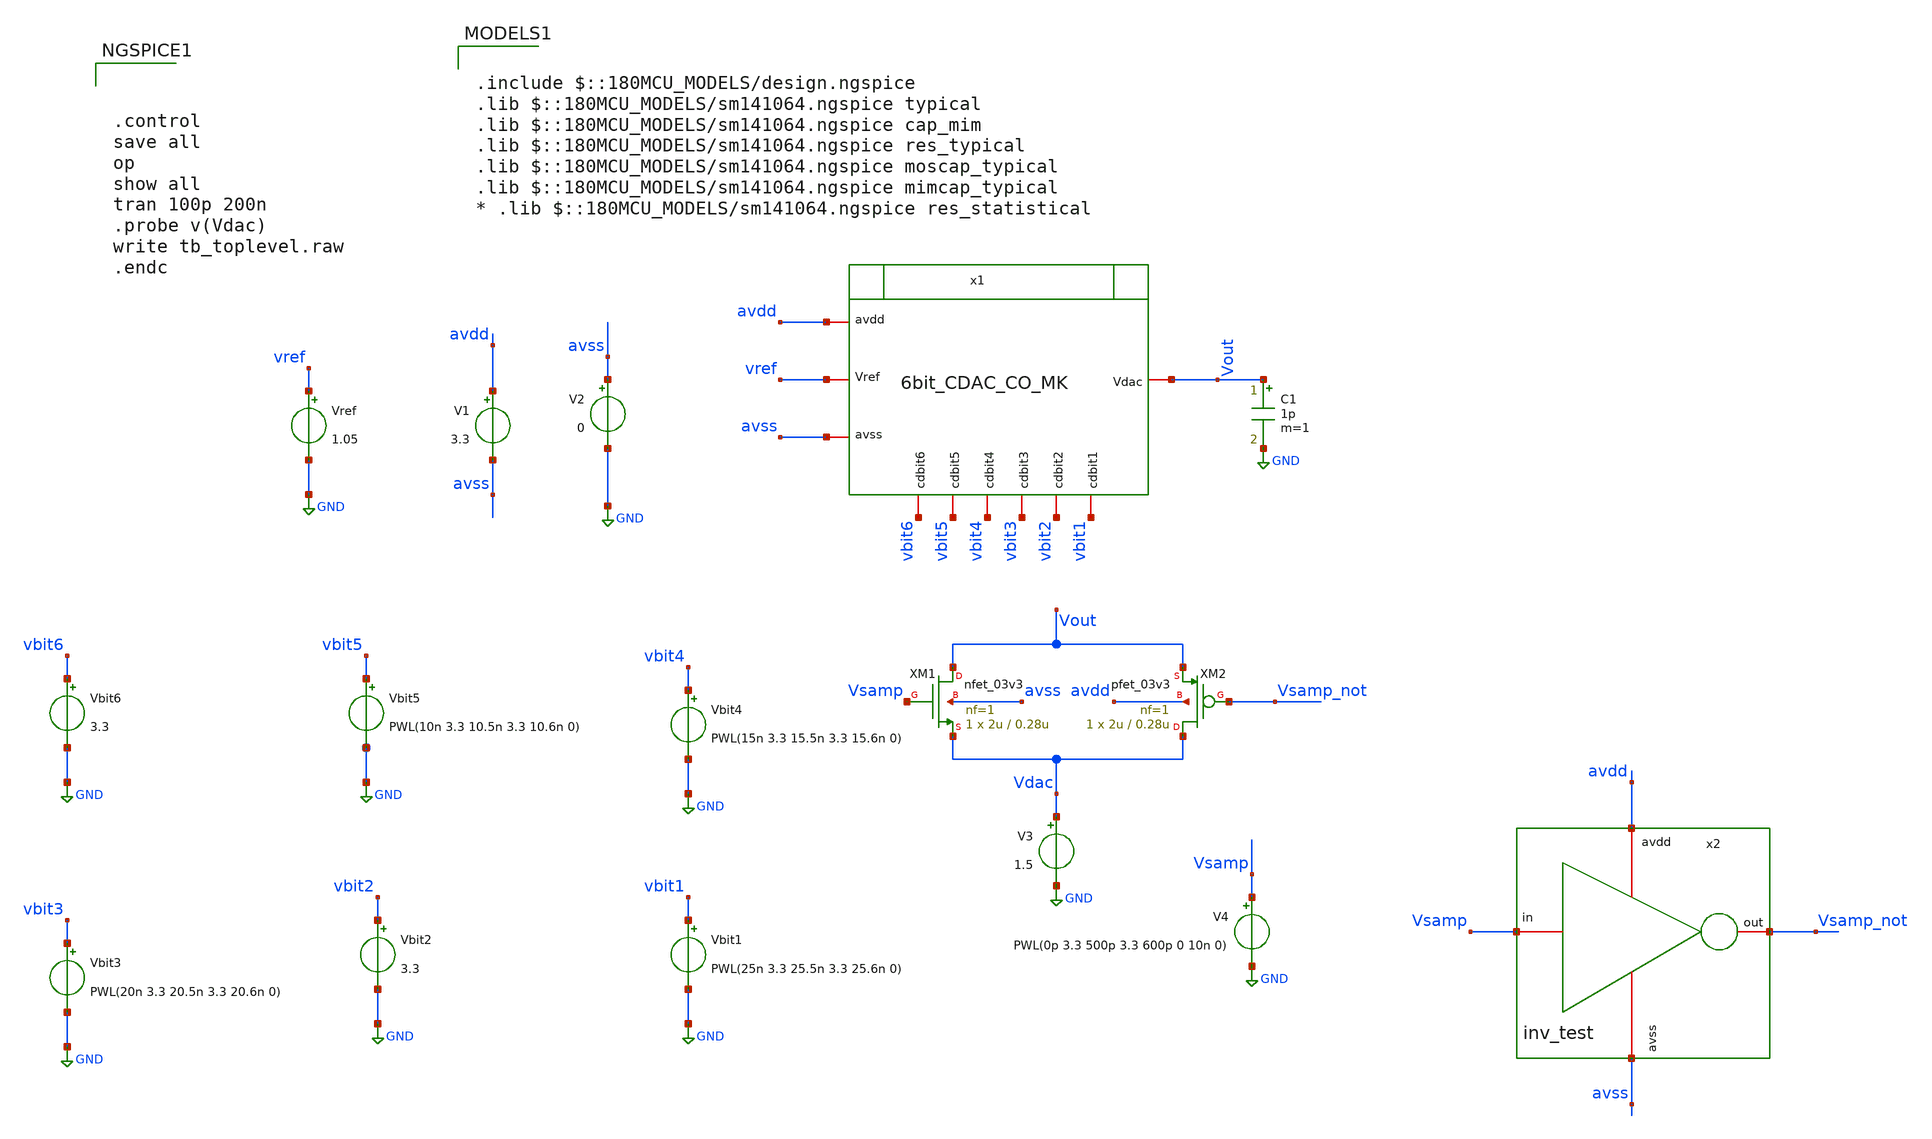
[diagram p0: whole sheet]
** sch_path: designs/full_ADC/tb_toplevel.sch
**.subckt tb_toplevel
V1 avdd avss 3.3
V2 avss GND 0
Vbit1 vbit1 GND PWL(25n 3.3 25.5n 3.3 25.6n 0)
Vbit2 vbit2 GND 3.3
Vbit3 vbit3 GND PWL(20n 3.3 20.5n 3.3 20.6n 0)
Vbit4 vbit4 GND PWL(15n 3.3 15.5n 3.3 15.6n 0)
Vbit5 vbit5 GND PWL(10n 3.3 10.5n 3.3 10.6n 0)
Vbit6 vbit6 GND 3.3
Vref vref GND 1.05
C1 Vout GND 1p m=1
V3 Vdac GND 1.5
XM1 Vout Vsamp Vdac avss nfet_03v3 L=0.28u W=2u nf=1 ad='int((nf+1)/2) * W/nf * 0.18u' as='int((nf+2)/2) * W/nf * 0.18u'
+ pd='2*int((nf+1)/2) * (W/nf + 0.18u)' ps='2*int((nf+2)/2) * (W/nf + 0.18u)' nrd='0.18u / W' nrs='0.18u / W'
+ sa=0 sb=0 sd=0 m=1
XM2 Vdac Vsamp_not Vout avdd pfet_03v3 L=0.28u W=2u nf=1 ad='int((nf+1)/2) * W/nf * 0.18u' as='int((nf+2)/2) * W/nf * 0.18u'
+ pd='2*int((nf+1)/2) * (W/nf + 0.18u)' ps='2*int((nf+2)/2) * (W/nf + 0.18u)' nrd='0.18u / W' nrs='0.18u / W'
+ sa=0 sb=0 sd=0 m=1
x2 avdd Vsamp Vsamp_not avss inv_test
V4 Vsamp GND PWL(0p 3.3 500p 3.3 600p 0 10n 0)
x1 Vout avdd avss vref vbit6 vbit5 vbit3 vbit1 vbit2 vbit4 6bit_CDAC_CO_MK
**** begin user architecture code



.control
save all
op
show all
tran 100p 200n
.probe v(Vdac)
write tb_toplevel.raw
.endc



.include $::180MCU_MODELS/design.ngspice
.lib $::180MCU_MODELS/sm141064.ngspice typical
.lib $::180MCU_MODELS/sm141064.ngspice cap_mim
.lib $::180MCU_MODELS/sm141064.ngspice res_typical
.lib $::180MCU_MODELS/sm141064.ngspice moscap_typical
.lib $::180MCU_MODELS/sm141064.ngspice mimcap_typical
* .lib $::180MCU_MODELS/sm141064.ngspice res_statistical

**** end user architecture code
**.ends

* expanding   symbol:  Wk_Chip_Odyssey/designs/libs/WK_Kadam/inv_test.sym # of pins=4
** sym_path: Wk_Chip_Odyssey/designs/libs/WK_Kadam/inv_test.sym
** sch_path: Wk_Chip_Odyssey/designs/libs/WK_Kadam/inv_test.sch
.subckt inv_test avdd in out avss
*.iopin avdd
*.iopin avss
*.iopin in
*.iopin out
XM3 out in avss avss nfet_03v3 L=0.28u W=1u nf=1 ad='int((nf+1)/2) * W/nf * 0.18u' as='int((nf+2)/2) * W/nf * 0.18u'
+ pd='2*int((nf+1)/2) * (W/nf + 0.18u)' ps='2*int((nf+2)/2) * (W/nf + 0.18u)' nrd='0.18u / W' nrs='0.18u / W'
+ sa=0 sb=0 sd=0 m=1
XM4 out in avdd avdd pfet_03v3 L=0.28u W=2.5u nf=1 ad='int((nf+1)/2) * W/nf * 0.18u' as='int((nf+2)/2) * W/nf * 0.18u'
+ pd='2*int((nf+1)/2) * (W/nf + 0.18u)' ps='2*int((nf+2)/2) * (W/nf + 0.18u)' nrd='0.18u / W' nrs='0.18u / W'
+ sa=0 sb=0 sd=0 m=1
.ends


* expanding   symbol:  Wk_Chip_Odyssey/designs/libs/WK_Kadam/6bit_CDAC_CO_MK.sym # of pins=10
** sym_path: designs/libs/WK_Kadam/6bit_CDAC_CO_MK.sym
** sch_path: designs/libs/WK_Kadam/6bit_CDAC_CO_MK.sch
.subckt 6bit_CDAC_CO_MK Vdac avdd avss Vref cdbit6 cdbit5 cdbit3 cdbit1 cdbit2 cdbit4
*.iopin Vref
*.iopin Vdac
*.iopin avdd
*.iopin avss
*.iopin cdbit6
*.iopin cdbit5
*.iopin cdbit4
*.iopin cdbit3
*.iopin cdbit2
*.iopin cdbit1
XC3 Vdac net2 cap_mim_2f0_m3m4_noshield c_width=10e-6 c_length=10e-6 m=4
XC4 Vdac net3 cap_mim_2f0_m3m4_noshield c_width=10e-6 c_length=10e-6 m=8
XC5 Vdac net4 cap_mim_2f0_m3m4_noshield c_width=10e-6 c_length=10e-6 m=16
XC6 Vdac net5 cap_mim_2f0_m3m4_noshield c_width=10e-6 c_length=10e-6 m=32
XC7 Vdac net6 cap_mim_2f0_m3m4_noshield c_width=10e-6 c_length=10e-6 m=64
x1 avdd avss net6 cdbit6 Vref c_dac1_switch
x2 avdd avss net5 cdbit5 Vref c_dac1_switch
x3 avdd avss net4 cdbit4 Vref c_dac1_switch
x4 avdd avss net3 cdbit3 Vref c_dac1_switch
x5 avdd avss net1 cdbit1 Vref c_dac1_switch
x6 avdd avss net2 cdbit2 Vref c_dac1_switch
XC1 Vdac avss cap_mim_2f0_m3m4_noshield c_width=10e-6 c_length=10e-6 m=2
XC2 Vdac net1 cap_mim_2f0_m3m4_noshield c_width=10e-6 c_length=10e-6 m=2
.ends


* expanding   symbol:  Wk_Chip_Odyssey/designs/libs/WK_Kadam/c_dac1_switch.sym # of pins=5
** sym_path: designs/libs/WK_Kadam/c_dac1_switch.sym
** sch_path: designs/libs/WK_Kadam/c_dac1_switch.sch
.subckt c_dac1_switch avdd avss sw_vout sw_bit sw_Vref
*.iopin avdd
*.iopin avss
*.iopin sw_bit
*.iopin sw_vout
*.iopin sw_Vref
XM1 sw_vout sw_bit sw_Vref avss nfet_03v3 L=0.28u W=2u nf=1 ad='int((nf+1)/2) * W/nf * 0.18u' as='int((nf+2)/2) * W/nf * 0.18u'
+ pd='2*int((nf+1)/2) * (W/nf + 0.18u)' ps='2*int((nf+2)/2) * (W/nf + 0.18u)' nrd='0.18u / W' nrs='0.18u / W'
+ sa=0 sb=0 sd=0 m=1
XM3 sw_vout net1 avss avss nfet_03v3 L=0.28u W=2u nf=1 ad='int((nf+1)/2) * W/nf * 0.18u' as='int((nf+2)/2) * W/nf * 0.18u'
+ pd='2*int((nf+1)/2) * (W/nf + 0.18u)' ps='2*int((nf+2)/2) * (W/nf + 0.18u)' nrd='0.18u / W' nrs='0.18u / W'
+ sa=0 sb=0 sd=0 m=1
XM4 avss sw_bit sw_vout avdd pfet_03v3 L=0.28u W=2u nf=1 ad='int((nf+1)/2) * W/nf * 0.18u' as='int((nf+2)/2) * W/nf * 0.18u'
+ pd='2*int((nf+1)/2) * (W/nf + 0.18u)' ps='2*int((nf+2)/2) * (W/nf + 0.18u)' nrd='0.18u / W' nrs='0.18u / W'
+ sa=0 sb=0 sd=0 m=1
XM2 sw_Vref net1 sw_vout avdd pfet_03v3 L=0.28u W=2u nf=1 ad='int((nf+1)/2) * W/nf * 0.18u' as='int((nf+2)/2) * W/nf * 0.18u'
+ pd='2*int((nf+1)/2) * (W/nf + 0.18u)' ps='2*int((nf+2)/2) * (W/nf + 0.18u)' nrd='0.18u / W' nrs='0.18u / W'
+ sa=0 sb=0 sd=0 m=1
x1v avdd sw_bit net1 avss inv_test
.ends

.GLOBAL GND
.end
